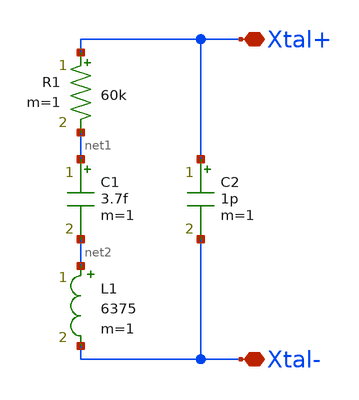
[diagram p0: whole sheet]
** sch_path: design/THESIS_EXP_RO_INVERTER_SKY130A/typical_xtal.sch
**.subckt typical_xtal Xtal+ Xtal-
*.iopin Xtal+
*.iopin Xtal-
R1 Xtal+ net1 60k m=1
C1 net1 net2 3.7f m=1
L1 net2 Xtal- 6375 m=1
C2 Xtal+ Xtal- 1p m=1
**.ends
.end
